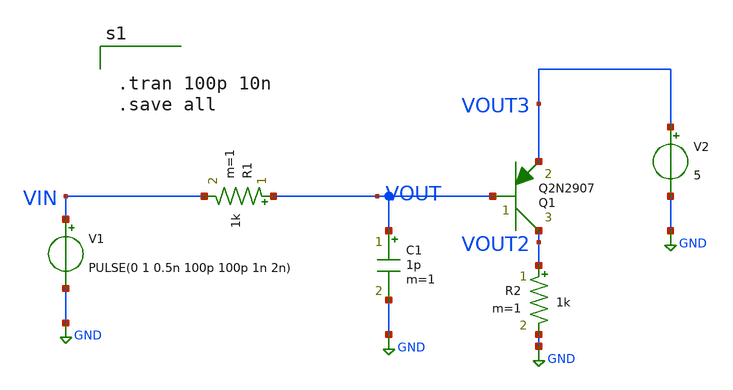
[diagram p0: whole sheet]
** sch_path: rc_ckt/rc_ckt2.sch
**.subckt rc_ckt2
R1 VOUT VIN 1k m=1
C1 VOUT GND 1p m=1
V1 VIN GND PULSE(0 1 0.5n 100p 100p 1n 2n)
Q1 VOUT2 VOUT VOUT3 Q2N2907 area=1 m=1
V2 VOUT3 GND 5
R2 VOUT2 GND 1k m=1
**** begin user architecture code


.tran 100p 10n
.save all


**** end user architecture code
**.ends
.GLOBAL GND
.end
